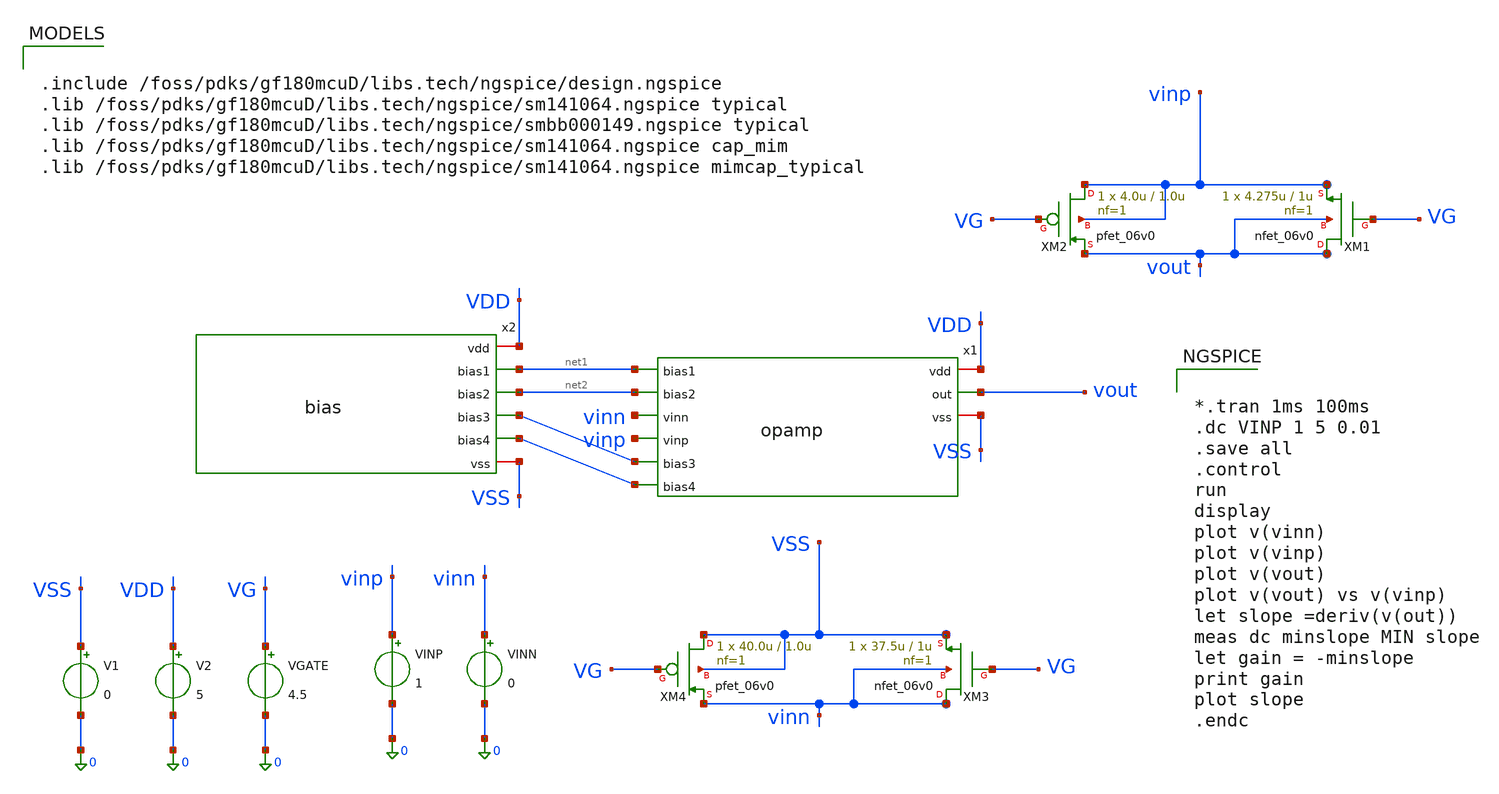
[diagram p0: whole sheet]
** sch_path: activities/opamp3An/OpAmpWFeedback.sch
**.subckt OpAmpWFeedback
x1 VDD net1 net2 vinn vout vinp net4 net3 VSS opamp
x2 VDD net1 net2 net4 net3 VSS bias
V1 VSS 0 0
V2 VDD 0 5
VGATE VG 0 4.5
VINP vinp 0 1
XM1 vout VG vinp vout nfet_06v0 L=1u W=4.275u nf=1 ad='int((nf+1)/2) * W/nf * 0.18u' as='int((nf+2)/2) * W/nf * 0.18u'
+ pd='2*int((nf+1)/2) * (W/nf + 0.18u)' ps='2*int((nf+2)/2) * (W/nf + 0.18u)' nrd='0.18u / W' nrs='0.18u / W'
+ sa=0 sb=0 sd=0 m=1
XM2 vinp VG vout vinp pfet_06v0 L=1.0u W=4.0u nf=1 ad='int((nf+1)/2) * W/nf * 0.18u' as='int((nf+2)/2) * W/nf * 0.18u'
+ pd='2*int((nf+1)/2) * (W/nf + 0.18u)' ps='2*int((nf+2)/2) * (W/nf + 0.18u)' nrd='0.18u / W' nrs='0.18u / W'
+ sa=0 sb=0 sd=0 m=1
XM3 vinn VG VSS vinn nfet_06v0 L=1u W=37.5u nf=1 ad='int((nf+1)/2) * W/nf * 0.18u' as='int((nf+2)/2) * W/nf * 0.18u'
+ pd='2*int((nf+1)/2) * (W/nf + 0.18u)' ps='2*int((nf+2)/2) * (W/nf + 0.18u)' nrd='0.18u / W' nrs='0.18u / W'
+ sa=0 sb=0 sd=0 m=1
XM4 VSS VG vinn VSS pfet_06v0 L=1.0u W=40.0u nf=1 ad='int((nf+1)/2) * W/nf * 0.18u' as='int((nf+2)/2) * W/nf * 0.18u'
+ pd='2*int((nf+1)/2) * (W/nf + 0.18u)' ps='2*int((nf+2)/2) * (W/nf + 0.18u)' nrd='0.18u / W' nrs='0.18u / W'
+ sa=0 sb=0 sd=0 m=1
VINN vinn 0 0
**** begin user architecture code


.include /foss/pdks/gf180mcuD/libs.tech/ngspice/design.ngspice
.lib /foss/pdks/gf180mcuD/libs.tech/ngspice/sm141064.ngspice typical
.lib /foss/pdks/gf180mcuD/libs.tech/ngspice/smbb000149.ngspice typical
.lib /foss/pdks/gf180mcuD/libs.tech/ngspice/sm141064.ngspice cap_mim
.lib /foss/pdks/gf180mcuD/libs.tech/ngspice/sm141064.ngspice mimcap_typical




*.tran 1ms 100ms
.dc VINP 1 5 0.01
.save all
.control
run
display
plot v(vinn)
plot v(vinp)
plot v(vout)
plot v(vout) vs v(vinp)
let slope =deriv(v(out))
meas dc minslope MIN slope
let gain = -minslope
print gain
plot slope
.endc


**** end user architecture code
**.ends
.end
